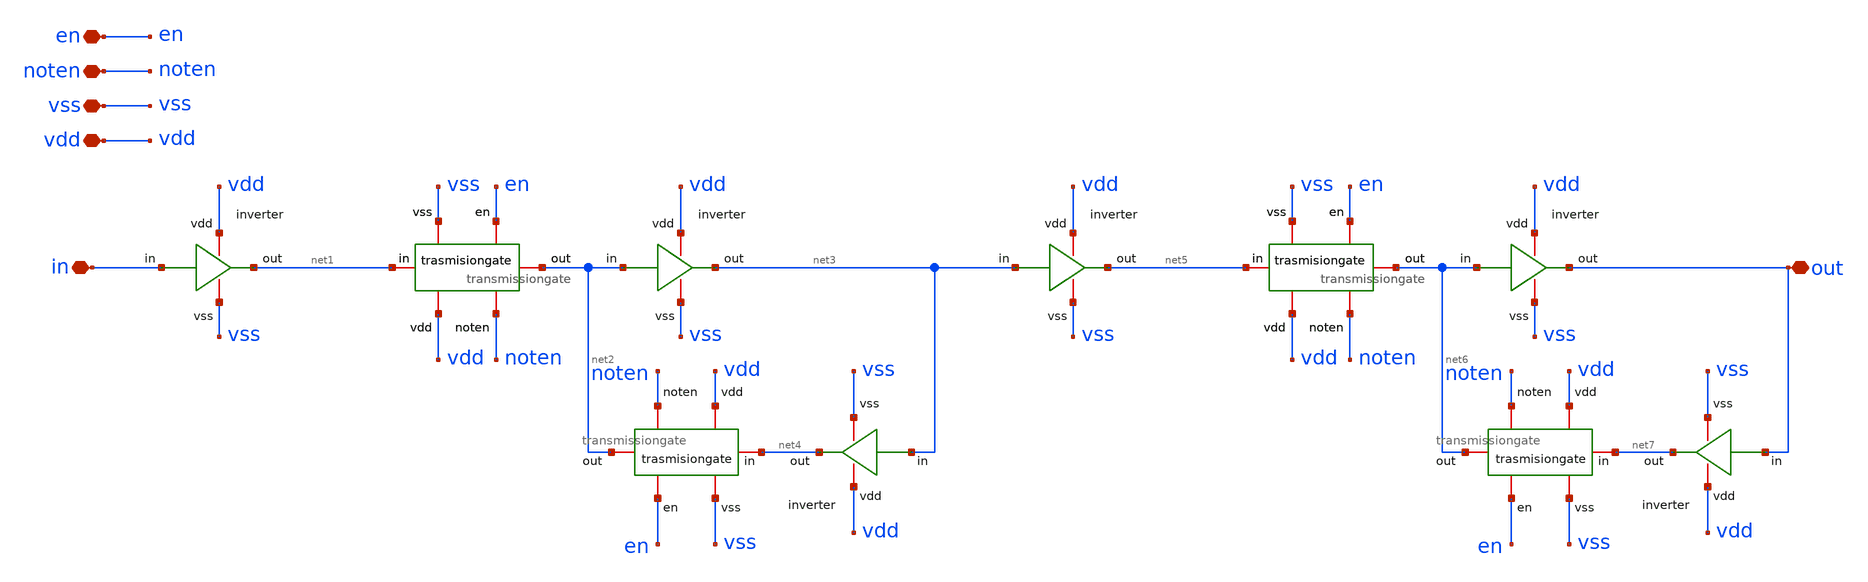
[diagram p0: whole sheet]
** sch_path: design/blocks/register/schematic/register.sch
**.subckt register in vdd vss out en noten
*.iopin in
*.iopin vdd
*.iopin vss
*.iopin out
*.iopin en
*.iopin noten
x1 vdd net1 in vss inverter
x2 net1 vdd noten net2 vss en transmissiongate
x3 vdd net3 net2 vss inverter
x4 vdd net4 net3 vss inverter
x5 net1 vdd noten net2 vss en transmissiongate
x6 net4 vdd noten net2 vss en transmissiongate
x7 vdd net5 net3 vss inverter
x8 net5 vdd noten net6 vss en transmissiongate
x9 vdd out net6 vss inverter
x10 vdd net7 out vss inverter
x11 net5 vdd noten net6 vss en transmissiongate
x12 net7 vdd noten net6 vss en transmissiongate
**.ends

* expanding   symbol:  blocks/inverter/schematic/inverter.sym # of pins=4
** sym_path: design/blocks/inverter/schematic/inverter.sym
** sch_path: design/blocks/inverter/schematic/inverter.sch
.subckt inverter vdd out in vss
*.iopin vdd
*.iopin out
*.iopin vss
*.iopin in
XM1 out in vss vss sky130_fd_pr__nfet_01v8 L=0.15 W=0.75 nf=1 ad='int((nf+1)/2) * W/nf * 0.29' as='int((nf+2)/2) * W/nf * 0.29'
+ pd='2*int((nf+1)/2) * (W/nf + 0.29)' ps='2*int((nf+2)/2) * (W/nf + 0.29)' nrd='0.29 / W' nrs='0.29 / W'
+ sa=0 sb=0 sd=0 mult=1 m=1
XM2 out in vdd vdd sky130_fd_pr__pfet_01v8 L=0.15 W=1.5 nf=1 ad='int((nf+1)/2) * W/nf * 0.29' as='int((nf+2)/2) * W/nf * 0.29'
+ pd='2*int((nf+1)/2) * (W/nf + 0.29)' ps='2*int((nf+2)/2) * (W/nf + 0.29)' nrd='0.29 / W' nrs='0.29 / W'
+ sa=0 sb=0 sd=0 mult=1 m=1
.ends


* expanding   symbol:  blocks/transmissiongate/schematic/transmissiongate.sym # of pins=6
** sym_path: design/blocks/transmissiongate/schematic/transmissiongate.sym
** sch_path: design/blocks/transmissiongate/schematic/transmissiongate.sch
.subckt transmissiongate in vdd noten out vss en
*.iopin noten
*.iopin en
*.iopin in
*.iopin out
*.iopin vdd
*.iopin vss
XM1 out noten in vdd sg13_lv_pmos w=1.5u l=0.15u ng=1 m=1 mm_ok=1
XM2 out en in vss sg13_lv_nmos w=0.75u l=0.15u ng=1 m=1 mm_ok=1
.ends

.end
